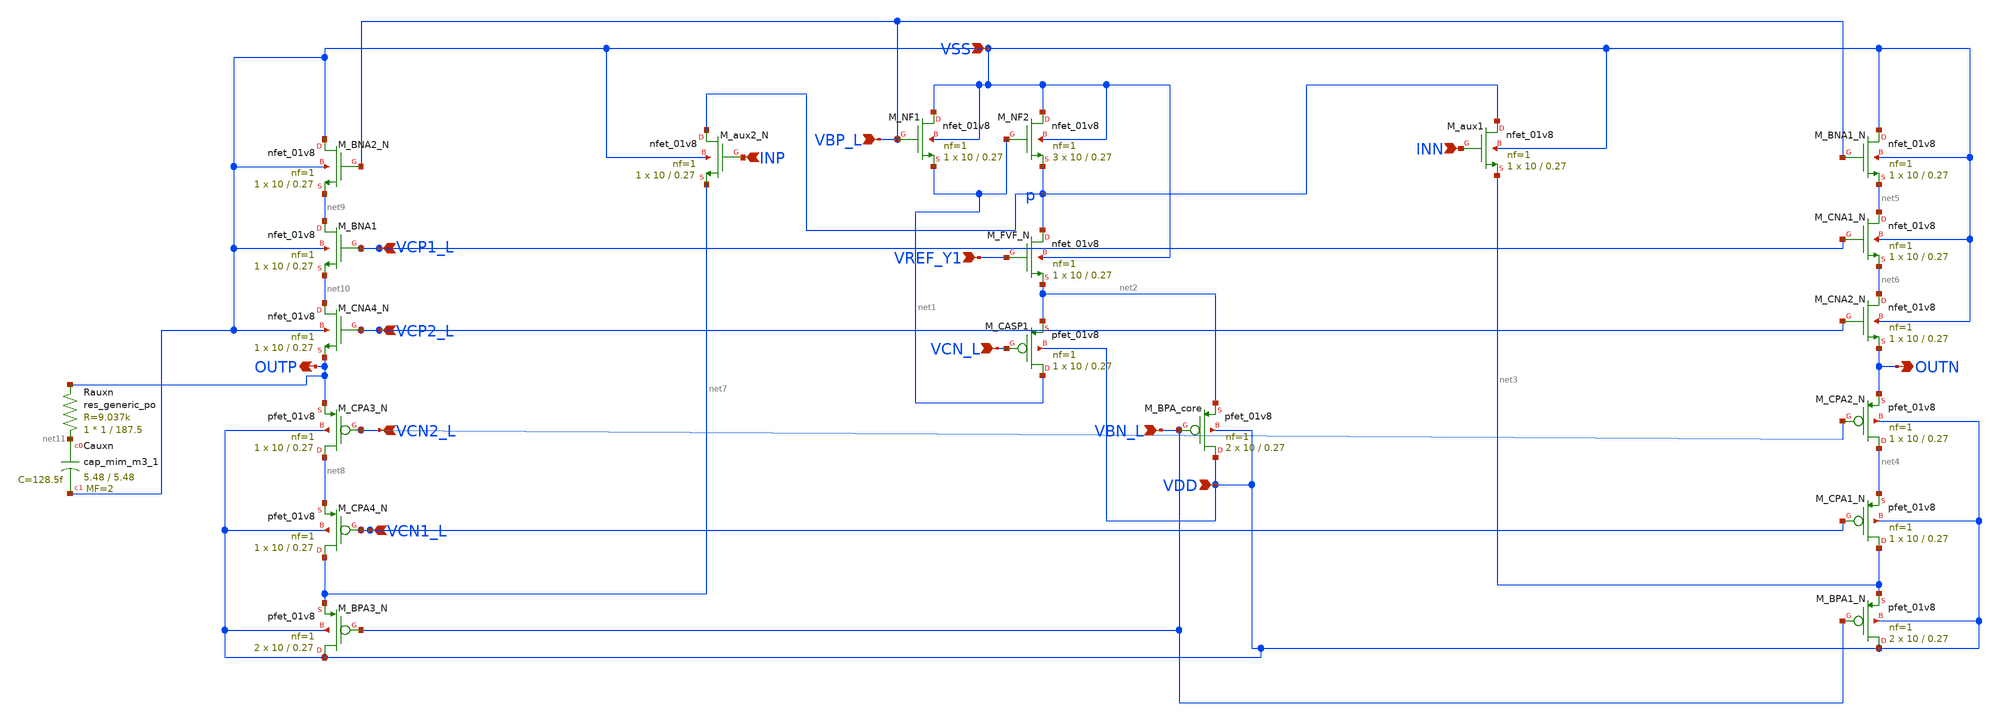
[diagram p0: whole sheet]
** sch_path: auxn.sch
**.subckt auxn VDD VSS VBN_L VCN_L VBP_L VREF_Y1 INN INP VCP1_L VCP2_L VCN1_L VCN2_L OUTP OUTN
*.ipin VDD
*.ipin VSS
*.ipin VBN_L
*.ipin VCN_L
*.ipin VBP_L
*.ipin VREF_Y1
*.ipin INN
*.ipin INP
*.ipin VCP1_L
*.ipin VCP2_L
*.ipin VCN1_L
*.ipin VCN2_L
*.opin OUTP
*.opin OUTN
XM_aux1 p INN net3 VSS sky130_fd_pr__nfet_01v8 L=0.27 W=10 nf=1 ad='int((1 + 1)/2) * 10 / 1 * 0.29' as='int((1 + 2)/2) * 10 / 1 * 0.29'
+ pd='2*int((1 + 1)/2) * (10 / 1 + 0.29)' ps='2*int((1 + 2)/2) * (10 / 1 + 0.29)' nrd='0.29 / 10 ' nrs='0.29 / 10 '
+ sa=0 sb=0 sd=0 mult=1 m=1
XM_CASP1 net1 VCN_L net2 VDD sky130_fd_pr__pfet_01v8 L=0.27 W=10 nf=1 ad='int((1 + 1)/2) * 10 / 1 * 0.29'
+ as='int((1 + 2)/2) * 10 / 1 * 0.29' pd='2*int((1 + 1)/2) * (10 / 1 + 0.29)' ps='2*int((1 + 2)/2) * (10 / 1 + 0.29)'
+ nrd='0.29 / 10 ' nrs='0.29 / 10 ' sa=0 sb=0 sd=0 mult=1 m=1
XM_CPA3_N net8 VCN2_L OUTP VDD sky130_fd_pr__pfet_01v8 L=0.27 W=10 nf=1 ad='int((1 + 1)/2) * 10 / 1 * 0.29'
+ as='int((1 + 2)/2) * 10 / 1 * 0.29' pd='2*int((1 + 1)/2) * (10 / 1 + 0.29)' ps='2*int((1 + 2)/2) * (10 / 1 + 0.29)'
+ nrd='0.29 / 10 ' nrs='0.29 / 10 ' sa=0 sb=0 sd=0 mult=1 m=1
XM_aux2_N p INP net7 VSS sky130_fd_pr__nfet_01v8 L=0.27 W=10 nf=1 ad='int((1 + 1)/2) * 10 / 1 * 0.29'
+ as='int((1 + 2)/2) * 10 / 1 * 0.29' pd='2*int((1 + 1)/2) * (10 / 1 + 0.29)' ps='2*int((1 + 2)/2) * (10 / 1 + 0.29)'
+ nrd='0.29 / 10 ' nrs='0.29 / 10 ' sa=0 sb=0 sd=0 mult=1 m=1
XM_NF2 VSS net1 p VSS sky130_fd_pr__nfet_01v8 L=0.27 W=10 nf=1 ad='int((1 + 1)/2) * 10 / 1 * 0.29' as='int((1 + 2)/2) * 10 / 1 * 0.29'
+ pd='2*int((1 + 1)/2) * (10 / 1 + 0.29)' ps='2*int((1 + 2)/2) * (10 / 1 + 0.29)' nrd='0.29 / 10 ' nrs='0.29 / 10 '
+ sa=0 sb=0 sd=0 mult=3 m=3
XM_BNA2_N VSS VBP_L net9 VSS sky130_fd_pr__nfet_01v8 L=0.27 W=10 nf=1 ad='int((1 + 1)/2) * 10 / 1 * 0.29'
+ as='int((1 + 2)/2) * 10 / 1 * 0.29' pd='2*int((1 + 1)/2) * (10 / 1 + 0.29)' ps='2*int((1 + 2)/2) * (10 / 1 + 0.29)'
+ nrd='0.29 / 10 ' nrs='0.29 / 10 ' sa=0 sb=0 sd=0 mult=1 m=1
XM_CNA4_N net10 VCP2_L OUTP VSS sky130_fd_pr__nfet_01v8 L=0.27 W=10 nf=1 ad='int((1 + 1)/2) * 10 / 1 * 0.29'
+ as='int((1 + 2)/2) * 10 / 1 * 0.29' pd='2*int((1 + 1)/2) * (10 / 1 + 0.29)' ps='2*int((1 + 2)/2) * (10 / 1 + 0.29)'
+ nrd='0.29 / 10 ' nrs='0.29 / 10 ' sa=0 sb=0 sd=0 mult=1 m=1
XM_CPA4_N net7 VCN1_L net8 VDD sky130_fd_pr__pfet_01v8 L=0.27 W=10 nf=1 ad='int((1 + 1)/2) * 10 / 1 * 0.29'
+ as='int((1 + 2)/2) * 10 / 1 * 0.29' pd='2*int((1 + 1)/2) * (10 / 1 + 0.29)' ps='2*int((1 + 2)/2) * (10 / 1 + 0.29)'
+ nrd='0.29 / 10 ' nrs='0.29 / 10 ' sa=0 sb=0 sd=0 mult=1 m=1
XM_BPA3_N VDD VBN_L net7 VDD sky130_fd_pr__pfet_01v8 L=0.27 W=10 nf=1 ad='int((1 + 1)/2) * 10 / 1 * 0.29'
+ as='int((1 + 2)/2) * 10 / 1 * 0.29' pd='2*int((1 + 1)/2) * (10 / 1 + 0.29)' ps='2*int((1 + 2)/2) * (10 / 1 + 0.29)'
+ nrd='0.29 / 10 ' nrs='0.29 / 10 ' sa=0 sb=0 sd=0 mult=2 m=2
XM_NF1 VSS VBP_L net1 VSS sky130_fd_pr__nfet_01v8 L=0.27 W=10 nf=1 ad='int((1 + 1)/2) * 10 / 1 * 0.29'
+ as='int((1 + 2)/2) * 10 / 1 * 0.29' pd='2*int((1 + 1)/2) * (10 / 1 + 0.29)' ps='2*int((1 + 2)/2) * (10 / 1 + 0.29)'
+ nrd='0.29 / 10 ' nrs='0.29 / 10 ' sa=0 sb=0 sd=0 mult=1 m=1
XM_FVF_N p VREF_Y1 net2 VSS sky130_fd_pr__nfet_01v8 L=0.27 W=10 nf=1 ad='int((1 + 1)/2) * 10 / 1 * 0.29'
+ as='int((1 + 2)/2) * 10 / 1 * 0.29' pd='2*int((1 + 1)/2) * (10 / 1 + 0.29)' ps='2*int((1 + 2)/2) * (10 / 1 + 0.29)'
+ nrd='0.29 / 10 ' nrs='0.29 / 10 ' sa=0 sb=0 sd=0 mult=1 m=1
XM_BPA_core VDD VBN_L net2 VDD sky130_fd_pr__pfet_01v8 L=0.27 W=10 nf=1 ad='int((1 + 1)/2) * 10 / 1 * 0.29'
+ as='int((1 + 2)/2) * 10 / 1 * 0.29' pd='2*int((1 + 1)/2) * (10 / 1 + 0.29)' ps='2*int((1 + 2)/2) * (10 / 1 + 0.29)'
+ nrd='0.29 / 10 ' nrs='0.29 / 10 ' sa=0 sb=0 sd=0 mult=2 m=2
XM_BNA1_N VSS VBP_L net5 VSS sky130_fd_pr__nfet_01v8 L=0.27 W=10 nf=1 ad='int((1 + 1)/2) * 10 / 1 * 0.29'
+ as='int((1 + 2)/2) * 10 / 1 * 0.29' pd='2*int((1 + 1)/2) * (10 / 1 + 0.29)' ps='2*int((1 + 2)/2) * (10 / 1 + 0.29)'
+ nrd='0.29 / 10 ' nrs='0.29 / 10 ' sa=0 sb=0 sd=0 mult=1 m=1
XM_CNA1_N net5 VCP1_L net6 VSS sky130_fd_pr__nfet_01v8 L=0.27 W=10 nf=1 ad='int((1 + 1)/2) * 10 / 1 * 0.29'
+ as='int((1 + 2)/2) * 10 / 1 * 0.29' pd='2*int((1 + 1)/2) * (10 / 1 + 0.29)' ps='2*int((1 + 2)/2) * (10 / 1 + 0.29)'
+ nrd='0.29 / 10 ' nrs='0.29 / 10 ' sa=0 sb=0 sd=0 mult=1 m=1
XM_CNA2_N net6 VCP2_L OUTN VSS sky130_fd_pr__nfet_01v8 L=0.27 W=10 nf=1 ad='int((1 + 1)/2) * 10 / 1 * 0.29'
+ as='int((1 + 2)/2) * 10 / 1 * 0.29' pd='2*int((1 + 1)/2) * (10 / 1 + 0.29)' ps='2*int((1 + 2)/2) * (10 / 1 + 0.29)'
+ nrd='0.29 / 10 ' nrs='0.29 / 10 ' sa=0 sb=0 sd=0 mult=1 m=1
XM_CPA2_N net4 VCN2_L OUTN VDD sky130_fd_pr__pfet_01v8 L=0.27 W=10 nf=1 ad='int((1 + 1)/2) * 10 / 1 * 0.29'
+ as='int((1 + 2)/2) * 10 / 1 * 0.29' pd='2*int((1 + 1)/2) * (10 / 1 + 0.29)' ps='2*int((1 + 2)/2) * (10 / 1 + 0.29)'
+ nrd='0.29 / 10 ' nrs='0.29 / 10 ' sa=0 sb=0 sd=0 mult=1 m=1
XM_CPA1_N net3 VCN1_L net4 VDD sky130_fd_pr__pfet_01v8 L=0.27 W=10 nf=1 ad='int((1 + 1)/2) * 10 / 1 * 0.29'
+ as='int((1 + 2)/2) * 10 / 1 * 0.29' pd='2*int((1 + 1)/2) * (10 / 1 + 0.29)' ps='2*int((1 + 2)/2) * (10 / 1 + 0.29)'
+ nrd='0.29 / 10 ' nrs='0.29 / 10 ' sa=0 sb=0 sd=0 mult=1 m=1
XM_BPA1_N VDD VBN_L net3 VDD sky130_fd_pr__pfet_01v8 L=0.27 W=10 nf=1 ad='int((1 + 1)/2) * 10 / 1 * 0.29'
+ as='int((1 + 2)/2) * 10 / 1 * 0.29' pd='2*int((1 + 1)/2) * (10 / 1 + 0.29)' ps='2*int((1 + 2)/2) * (10 / 1 + 0.29)'
+ nrd='0.29 / 10 ' nrs='0.29 / 10 ' sa=0 sb=0 sd=0 mult=2 m=2
XCauxn net11 VSS sky130_fd_pr__cap_mim_m3_1 W=5.48 L=5.48 MF=2 m=2
XRauxn net11 OUTP sky130_fd_pr__res_generic_po W=1 L=187.5 m=1
XM_BNA1 net9 VCP1_L net10 VSS sky130_fd_pr__nfet_01v8 L=0.27 W=10 nf=1 ad='int((1 + 1)/2) * 10 / 1 * 0.29'
+ as='int((1 + 2)/2) * 10 / 1 * 0.29' pd='2*int((1 + 1)/2) * (10 / 1 + 0.29)' ps='2*int((1 + 2)/2) * (10 / 1 + 0.29)'
+ nrd='0.29 / 10 ' nrs='0.29 / 10 ' sa=0 sb=0 sd=0 mult=1 m=1
**.ends
.end
